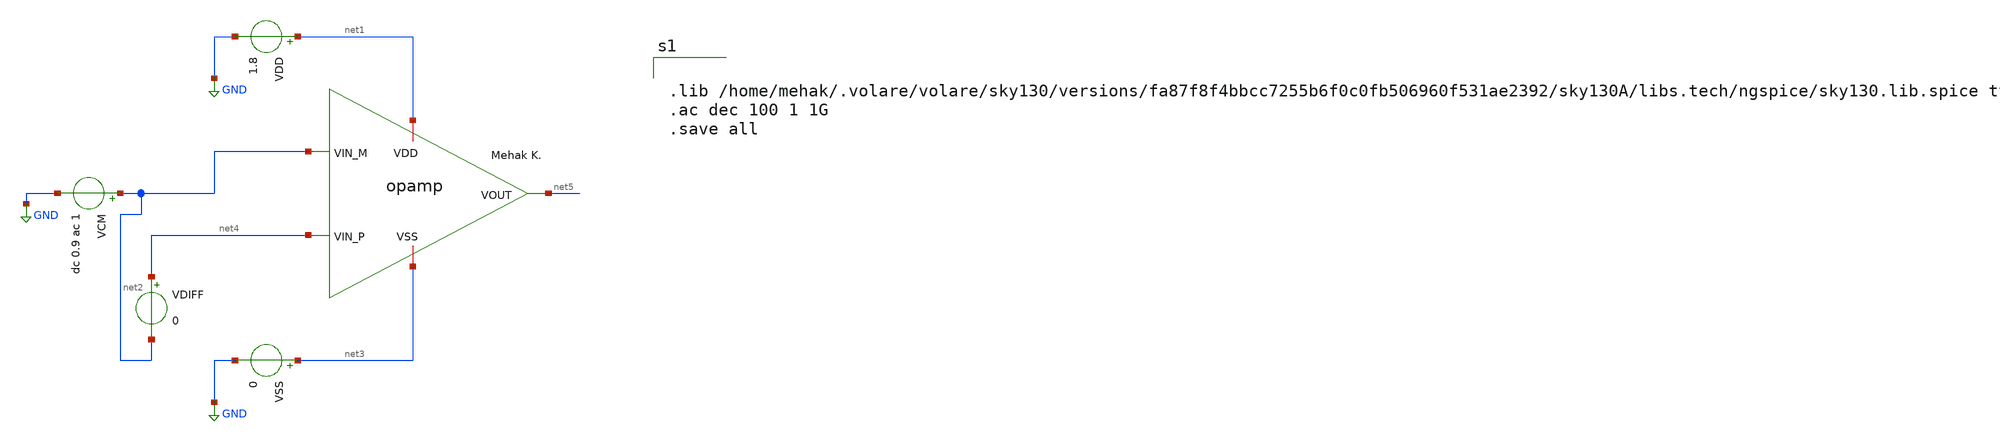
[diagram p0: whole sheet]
** sch_path: analog/build/schematic/tb_cmrr.sch
**.subckt tb_cmrr
VDD net1 GND 1.8
VSS net3 GND 0
VCM net2 GND dc 0.9 ac 1
VDIFF net4 net2 0
x1 net1 net5 net2 net4 net3 opamp_two_stage
**** begin user architecture code


.lib /home/mehak/.volare/volare/sky130/versions/fa87f8f4bbcc7255b6f0c0fb506960f531ae2392/sky130A/libs.tech/ngspice/sky130.lib.spice tt
.ac dec 100 1 1G
.save all


**** end user architecture code
**.ends
.GLOBAL GND
.end
